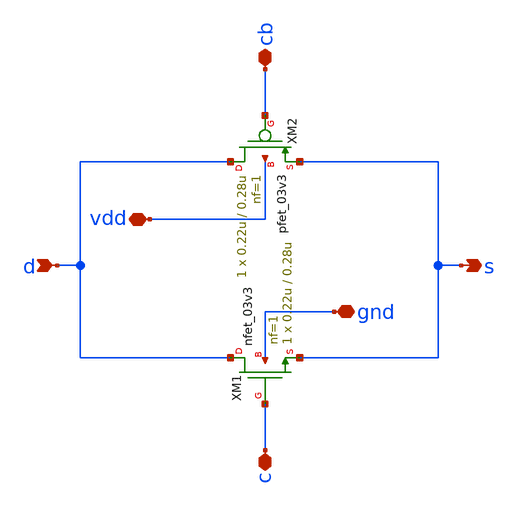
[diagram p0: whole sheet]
** sch_path: transgate.sch
**.subckt transgate gnd vdd cb c d s
*.iopin gnd
*.iopin vdd
*.iopin cb
*.iopin c
*.ipin d
*.opin s
XM1 d c s gnd nfet_03v3 L=0.28u W=0.22u nf=1 ad='int((nf+1)/2) * W/nf * 0.18u' as='int((nf+2)/2) * W/nf * 0.18u'
+ pd='2*int((nf+1)/2) * (W/nf + 0.18u)' ps='2*int((nf+2)/2) * (W/nf + 0.18u)' nrd='0.18u / W' nrs='0.18u / W'
+ sa=0 sb=0 sd=0 m=1
XM2 d cb s vdd pfet_03v3 L=0.28u W=0.22u nf=1 ad='int((nf+1)/2) * W/nf * 0.18u' as='int((nf+2)/2) * W/nf * 0.18u'
+ pd='2*int((nf+1)/2) * (W/nf + 0.18u)' ps='2*int((nf+2)/2) * (W/nf + 0.18u)' nrd='0.18u / W' nrs='0.18u / W'
+ sa=0 sb=0 sd=0 m=1
**.ends
.end
